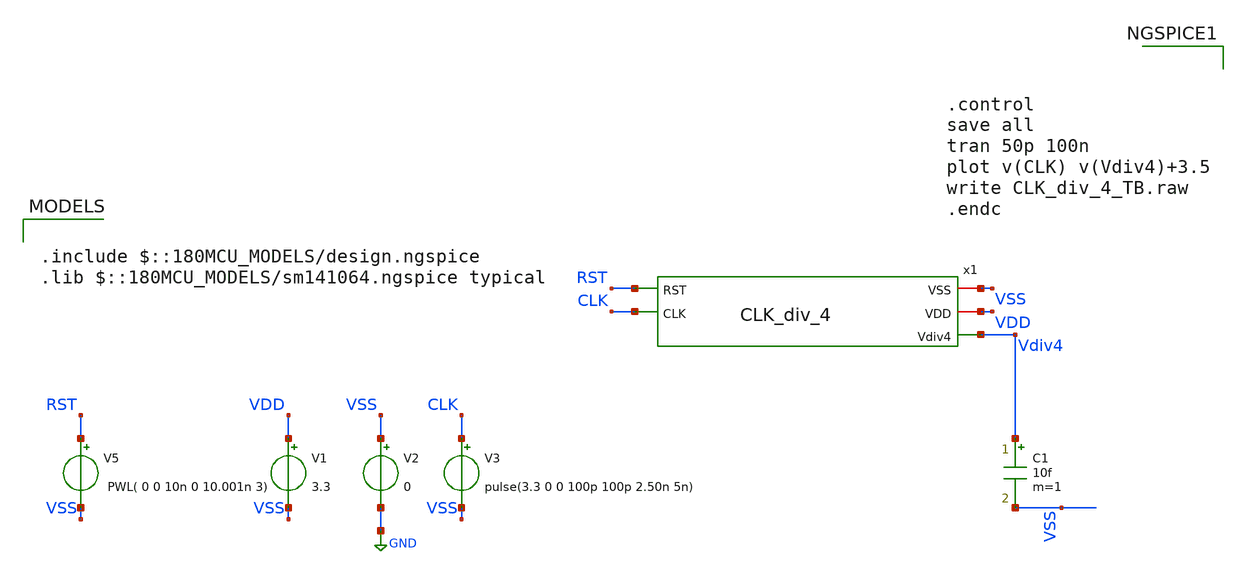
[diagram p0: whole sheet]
** sch_path: Clock_Generator_PAKISTAN_02/xschem/CLK_div_4_TB.sch
**.subckt CLK_div_4_TB
V1 VDD VSS 3.3
V2 VSS GND 0
V3 CLK VSS pulse(3.3 0 0 100p 100p 2.50n 5n)
C1 Vdiv4 VSS 10f m=1
V5 RST VSS PWL( 0 0 10n 0 10.001n 3)
x1 VSS VDD Vdiv4 RST CLK CLK_div_4
**** begin user architecture code

.include $::180MCU_MODELS/design.ngspice
.lib $::180MCU_MODELS/sm141064.ngspice typical




.control
save all
tran 50p 100n
plot v(CLK) v(Vdiv4)+3.5
write CLK_div_4_TB.raw
.endc


**** end user architecture code
**.ends
.GLOBAL GND
.end
